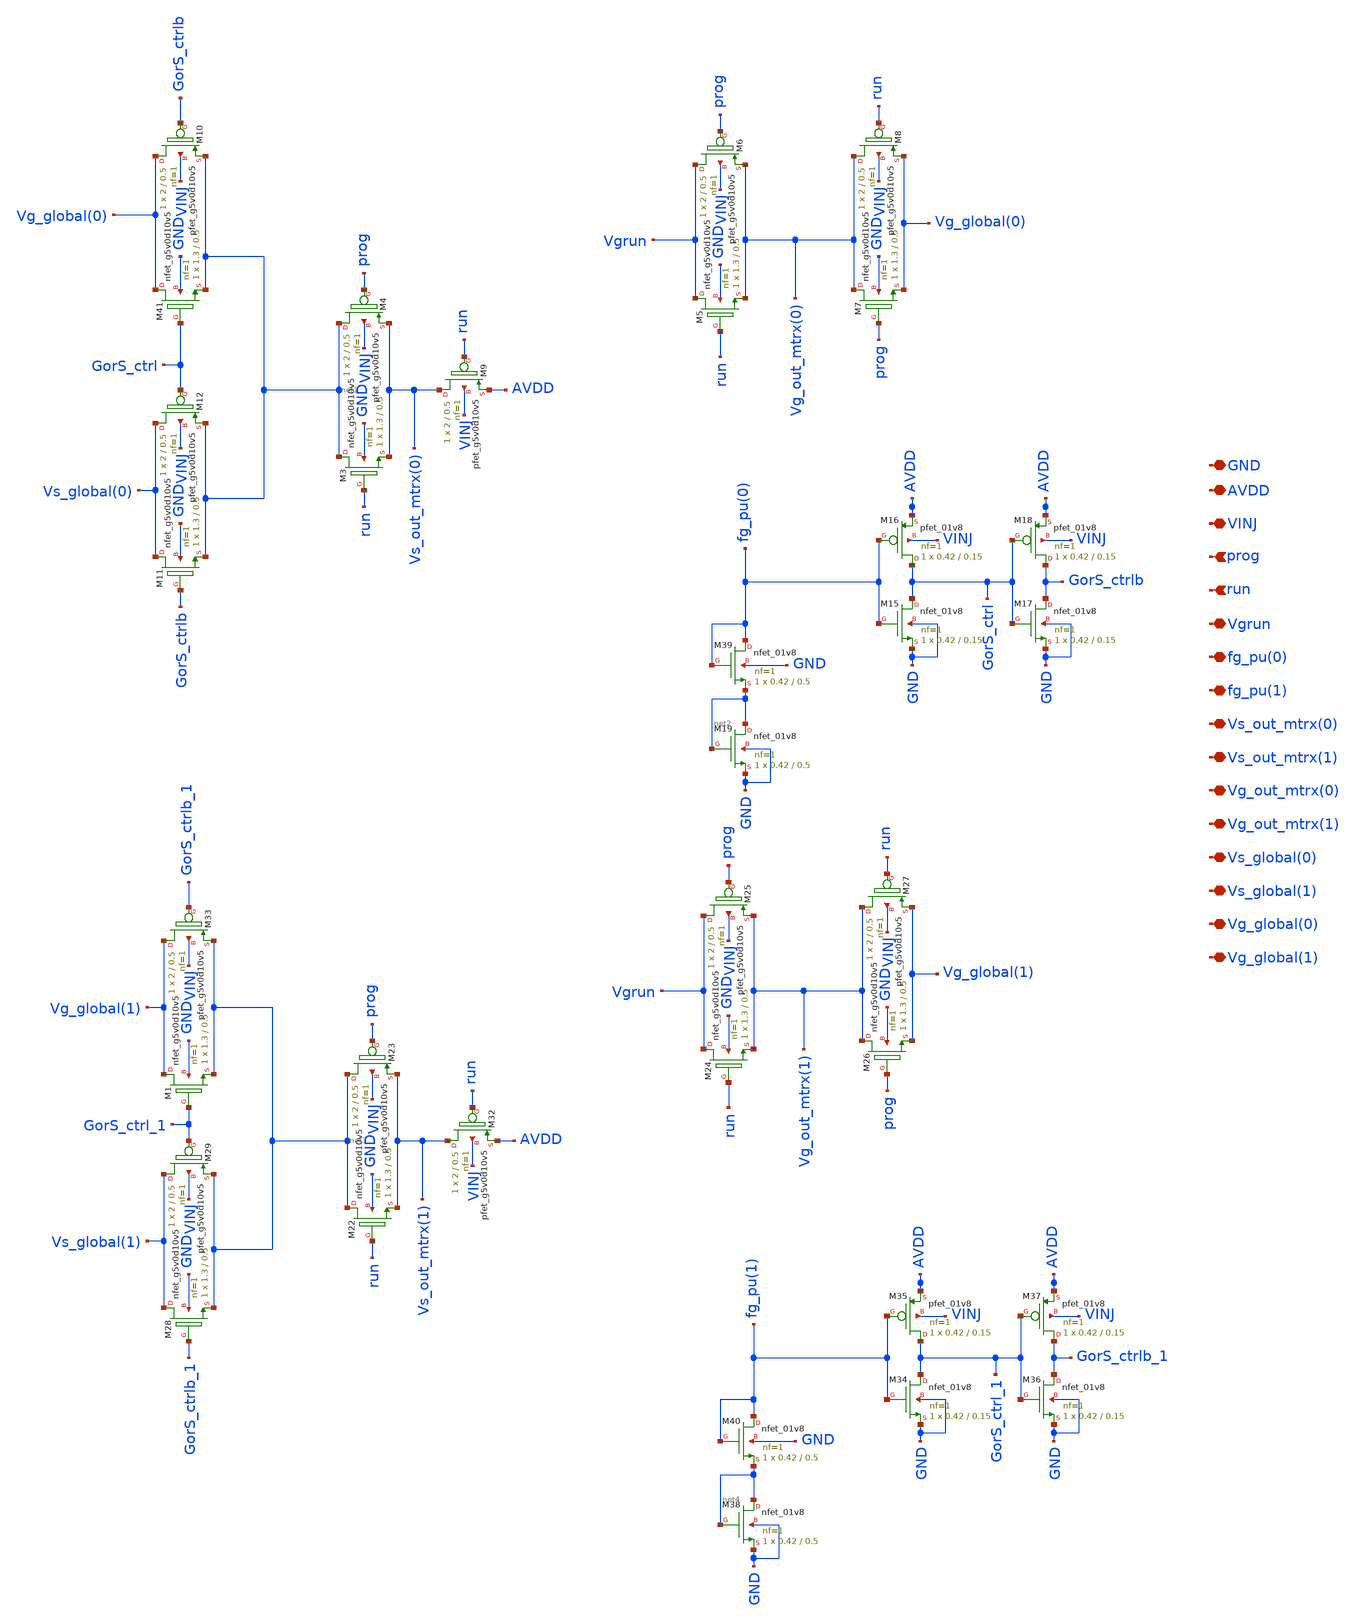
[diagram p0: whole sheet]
** sch_path: sky130_cells/IndirctGswc_OutMat/IndirectGswc_OutMatSchem.sch
**.subckt IndirectGswc_OutMatSchem GND AVDD VINJ Vgrun fg_pu(0) fg_pu(1) Vs_out_mtrx(0)
*+ Vs_out_mtrx(1) Vg_out_mtrx(0) Vg_out_mtrx(1) Vg_global(0) Vg_global(1) prog run Vs_global(0) Vs_global(1)
*.iopin GND
*.iopin AVDD
*.iopin VINJ
*.iopin Vgrun
*.iopin fg_pu(0)
*.iopin fg_pu(1)
*.iopin Vs_out_mtrx(0)
*.iopin Vs_out_mtrx(1)
*.iopin Vg_out_mtrx(0)
*.iopin Vg_out_mtrx(1)
*.iopin Vg_global(0)
*.iopin Vg_global(1)
*.ipin prog
*.ipin run
*.iopin Vs_global(0)
*.iopin Vs_global(1)
XM3 net1 run Vs_out_mtrx(0) GND sky130_fd_pr__nfet_g5v0d10v5 L=0.5 W=1.3 nf=1 ad='int((1 + 1)/2) * 1.3 / 1 * 0.29'
+ as='int((1 + 2)/2) * 1.3 / 1 * 0.29' pd='2*int((1 + 1)/2) * (1.3 / 1 + 0.29)' ps='2*int((1 + 2)/2) * (1.3 / 1 + 0.29)'
+ nrd='0.29 / 1.3 ' nrs='0.29 / 1.3 ' sa=0 sb=0 sd=0 mult=1 m=1
XM4 net1 prog Vs_out_mtrx(0) VINJ sky130_fd_pr__pfet_g5v0d10v5 L=0.5 W=2 nf=1 ad='int((1 + 1)/2) * 2 / 1 * 0.29'
+ as='int((1 + 2)/2) * 2 / 1 * 0.29' pd='2*int((1 + 1)/2) * (2 / 1 + 0.29)' ps='2*int((1 + 2)/2) * (2 / 1 + 0.29)'
+ nrd='0.29 / 2 ' nrs='0.29 / 2 ' sa=0 sb=0 sd=0 mult=1 m=1
XM5 Vgrun run Vg_out_mtrx(0) GND sky130_fd_pr__nfet_g5v0d10v5 L=0.5 W=1.3 nf=1 ad='int((1 + 1)/2) * 1.3 / 1 * 0.29'
+ as='int((1 + 2)/2) * 1.3 / 1 * 0.29' pd='2*int((1 + 1)/2) * (1.3 / 1 + 0.29)' ps='2*int((1 + 2)/2) * (1.3 / 1 + 0.29)'
+ nrd='0.29 / 1.3 ' nrs='0.29 / 1.3 ' sa=0 sb=0 sd=0 mult=1 m=1
XM6 Vgrun prog Vg_out_mtrx(0) VINJ sky130_fd_pr__pfet_g5v0d10v5 L=0.5 W=2 nf=1 ad='int((1 + 1)/2) * 2 / 1 * 0.29'
+ as='int((1 + 2)/2) * 2 / 1 * 0.29' pd='2*int((1 + 1)/2) * (2 / 1 + 0.29)' ps='2*int((1 + 2)/2) * (2 / 1 + 0.29)'
+ nrd='0.29 / 2 ' nrs='0.29 / 2 ' sa=0 sb=0 sd=0 mult=1 m=1
XM7 Vg_out_mtrx(0) prog Vg_global(0) GND sky130_fd_pr__nfet_g5v0d10v5 L=0.5 W=1.3 nf=1 ad='int((1 + 1)/2) * 1.3 / 1 * 0.29'
+ as='int((1 + 2)/2) * 1.3 / 1 * 0.29' pd='2*int((1 + 1)/2) * (1.3 / 1 + 0.29)' ps='2*int((1 + 2)/2) * (1.3 / 1 + 0.29)'
+ nrd='0.29 / 1.3 ' nrs='0.29 / 1.3 ' sa=0 sb=0 sd=0 mult=1 m=1
XM8 Vg_out_mtrx(0) run Vg_global(0) VINJ sky130_fd_pr__pfet_g5v0d10v5 L=0.5 W=2 nf=1 ad='int((1 + 1)/2) * 2 / 1 * 0.29'
+ as='int((1 + 2)/2) * 2 / 1 * 0.29' pd='2*int((1 + 1)/2) * (2 / 1 + 0.29)' ps='2*int((1 + 2)/2) * (2 / 1 + 0.29)'
+ nrd='0.29 / 2 ' nrs='0.29 / 2 ' sa=0 sb=0 sd=0 mult=1 m=1
XM11 Vs_global(0) GorS_ctrlb net1 GND sky130_fd_pr__nfet_g5v0d10v5 L=0.5 W=1.3 nf=1 ad='int((1 + 1)/2) * 1.3 / 1 * 0.29'
+ as='int((1 + 2)/2) * 1.3 / 1 * 0.29' pd='2*int((1 + 1)/2) * (1.3 / 1 + 0.29)' ps='2*int((1 + 2)/2) * (1.3 / 1 + 0.29)'
+ nrd='0.29 / 1.3 ' nrs='0.29 / 1.3 ' sa=0 sb=0 sd=0 mult=1 m=1
XM12 Vs_global(0) GorS_ctrl net1 VINJ sky130_fd_pr__pfet_g5v0d10v5 L=0.5 W=2 nf=1 ad='int((1 + 1)/2) * 2 / 1 * 0.29'
+ as='int((1 + 2)/2) * 2 / 1 * 0.29' pd='2*int((1 + 1)/2) * (2 / 1 + 0.29)' ps='2*int((1 + 2)/2) * (2 / 1 + 0.29)'
+ nrd='0.29 / 2 ' nrs='0.29 / 2 ' sa=0 sb=0 sd=0 mult=1 m=1
XM9 Vs_out_mtrx(0) run AVDD VINJ sky130_fd_pr__pfet_g5v0d10v5 L=0.5 W=2 nf=1 ad='int((1 + 1)/2) * 2 / 1 * 0.29'
+ as='int((1 + 2)/2) * 2 / 1 * 0.29' pd='2*int((1 + 1)/2) * (2 / 1 + 0.29)' ps='2*int((1 + 2)/2) * (2 / 1 + 0.29)'
+ nrd='0.29 / 2 ' nrs='0.29 / 2 ' sa=0 sb=0 sd=0 mult=1 m=1
XM10 Vg_global(0) GorS_ctrlb net1 VINJ sky130_fd_pr__pfet_g5v0d10v5 L=0.5 W=2 nf=1 ad='int((1 + 1)/2) * 2 / 1 * 0.29'
+ as='int((1 + 2)/2) * 2 / 1 * 0.29' pd='2*int((1 + 1)/2) * (2 / 1 + 0.29)' ps='2*int((1 + 2)/2) * (2 / 1 + 0.29)'
+ nrd='0.29 / 2 ' nrs='0.29 / 2 ' sa=0 sb=0 sd=0 mult=1 m=1
XM15 GorS_ctrl fg_pu(0) GND GND sky130_fd_pr__nfet_01v8 L=0.15 W=0.42 nf=1 ad='int((1 + 1)/2) * 0.42 / 1 * 0.29'
+ as='int((1 + 2)/2) * 0.42 / 1 * 0.29' pd='2*int((1 + 1)/2) * (0.42 / 1 + 0.29)' ps='2*int((1 + 2)/2) * (0.42 / 1 + 0.29)'
+ nrd='0.29 / 0.42 ' nrs='0.29 / 0.42 ' sa=0 sb=0 sd=0 mult=1 m=1
XM16 GorS_ctrl fg_pu(0) AVDD VINJ sky130_fd_pr__pfet_01v8 L=0.15 W=0.42 nf=1 ad='int((1 + 1)/2) * 0.42 / 1 * 0.29'
+ as='int((1 + 2)/2) * 0.42 / 1 * 0.29' pd='2*int((1 + 1)/2) * (0.42 / 1 + 0.29)' ps='2*int((1 + 2)/2) * (0.42 / 1 + 0.29)'
+ nrd='0.29 / 0.42 ' nrs='0.29 / 0.42 ' sa=0 sb=0 sd=0 mult=1 m=1
XM19 net2 net2 GND GND sky130_fd_pr__nfet_01v8 L=0.5 W=0.42 nf=1 ad='int((1 + 1)/2) * 0.42 / 1 * 0.29'
+ as='int((1 + 2)/2) * 0.42 / 1 * 0.29' pd='2*int((1 + 1)/2) * (0.42 / 1 + 0.29)' ps='2*int((1 + 2)/2) * (0.42 / 1 + 0.29)'
+ nrd='0.29 / 0.42 ' nrs='0.29 / 0.42 ' sa=0 sb=0 sd=0 mult=1 m=1
XM22 net3 run Vs_out_mtrx(1) GND sky130_fd_pr__nfet_g5v0d10v5 L=0.5 W=1.3 nf=1 ad='int((1 + 1)/2) * 1.3 / 1 * 0.29'
+ as='int((1 + 2)/2) * 1.3 / 1 * 0.29' pd='2*int((1 + 1)/2) * (1.3 / 1 + 0.29)' ps='2*int((1 + 2)/2) * (1.3 / 1 + 0.29)'
+ nrd='0.29 / 1.3 ' nrs='0.29 / 1.3 ' sa=0 sb=0 sd=0 mult=1 m=1
XM23 net3 prog Vs_out_mtrx(1) VINJ sky130_fd_pr__pfet_g5v0d10v5 L=0.5 W=2 nf=1 ad='int((1 + 1)/2) * 2 / 1 * 0.29'
+ as='int((1 + 2)/2) * 2 / 1 * 0.29' pd='2*int((1 + 1)/2) * (2 / 1 + 0.29)' ps='2*int((1 + 2)/2) * (2 / 1 + 0.29)'
+ nrd='0.29 / 2 ' nrs='0.29 / 2 ' sa=0 sb=0 sd=0 mult=1 m=1
XM24 Vgrun run Vg_out_mtrx(1) GND sky130_fd_pr__nfet_g5v0d10v5 L=0.5 W=1.3 nf=1 ad='int((1 + 1)/2) * 1.3 / 1 * 0.29'
+ as='int((1 + 2)/2) * 1.3 / 1 * 0.29' pd='2*int((1 + 1)/2) * (1.3 / 1 + 0.29)' ps='2*int((1 + 2)/2) * (1.3 / 1 + 0.29)'
+ nrd='0.29 / 1.3 ' nrs='0.29 / 1.3 ' sa=0 sb=0 sd=0 mult=1 m=1
XM25 Vgrun prog Vg_out_mtrx(1) VINJ sky130_fd_pr__pfet_g5v0d10v5 L=0.5 W=2 nf=1 ad='int((1 + 1)/2) * 2 / 1 * 0.29'
+ as='int((1 + 2)/2) * 2 / 1 * 0.29' pd='2*int((1 + 1)/2) * (2 / 1 + 0.29)' ps='2*int((1 + 2)/2) * (2 / 1 + 0.29)'
+ nrd='0.29 / 2 ' nrs='0.29 / 2 ' sa=0 sb=0 sd=0 mult=1 m=1
XM26 Vg_out_mtrx(1) prog Vg_global(1) GND sky130_fd_pr__nfet_g5v0d10v5 L=0.5 W=1.3 nf=1 ad='int((1 + 1)/2) * 1.3 / 1 * 0.29'
+ as='int((1 + 2)/2) * 1.3 / 1 * 0.29' pd='2*int((1 + 1)/2) * (1.3 / 1 + 0.29)' ps='2*int((1 + 2)/2) * (1.3 / 1 + 0.29)'
+ nrd='0.29 / 1.3 ' nrs='0.29 / 1.3 ' sa=0 sb=0 sd=0 mult=1 m=1
XM27 Vg_out_mtrx(1) run Vg_global(1) VINJ sky130_fd_pr__pfet_g5v0d10v5 L=0.5 W=2 nf=1 ad='int((1 + 1)/2) * 2 / 1 * 0.29'
+ as='int((1 + 2)/2) * 2 / 1 * 0.29' pd='2*int((1 + 1)/2) * (2 / 1 + 0.29)' ps='2*int((1 + 2)/2) * (2 / 1 + 0.29)'
+ nrd='0.29 / 2 ' nrs='0.29 / 2 ' sa=0 sb=0 sd=0 mult=1 m=1
XM28 Vs_global(1) GorS_ctrlb_1 net3 GND sky130_fd_pr__nfet_g5v0d10v5 L=0.5 W=1.3 nf=1 ad='int((1 + 1)/2) * 1.3 / 1 * 0.29'
+ as='int((1 + 2)/2) * 1.3 / 1 * 0.29' pd='2*int((1 + 1)/2) * (1.3 / 1 + 0.29)' ps='2*int((1 + 2)/2) * (1.3 / 1 + 0.29)'
+ nrd='0.29 / 1.3 ' nrs='0.29 / 1.3 ' sa=0 sb=0 sd=0 mult=1 m=1
XM29 Vs_global(1) GorS_ctrl_1 net3 VINJ sky130_fd_pr__pfet_g5v0d10v5 L=0.5 W=2 nf=1 ad='int((1 + 1)/2) * 2 / 1 * 0.29'
+ as='int((1 + 2)/2) * 2 / 1 * 0.29' pd='2*int((1 + 1)/2) * (2 / 1 + 0.29)' ps='2*int((1 + 2)/2) * (2 / 1 + 0.29)'
+ nrd='0.29 / 2 ' nrs='0.29 / 2 ' sa=0 sb=0 sd=0 mult=1 m=1
XM32 Vs_out_mtrx(1) run AVDD VINJ sky130_fd_pr__pfet_g5v0d10v5 L=0.5 W=2 nf=1 ad='int((1 + 1)/2) * 2 / 1 * 0.29'
+ as='int((1 + 2)/2) * 2 / 1 * 0.29' pd='2*int((1 + 1)/2) * (2 / 1 + 0.29)' ps='2*int((1 + 2)/2) * (2 / 1 + 0.29)'
+ nrd='0.29 / 2 ' nrs='0.29 / 2 ' sa=0 sb=0 sd=0 mult=1 m=1
XM33 Vg_global(1) GorS_ctrlb_1 net3 VINJ sky130_fd_pr__pfet_g5v0d10v5 L=0.5 W=2 nf=1 ad='int((1 + 1)/2) * 2 / 1 * 0.29'
+ as='int((1 + 2)/2) * 2 / 1 * 0.29' pd='2*int((1 + 1)/2) * (2 / 1 + 0.29)' ps='2*int((1 + 2)/2) * (2 / 1 + 0.29)'
+ nrd='0.29 / 2 ' nrs='0.29 / 2 ' sa=0 sb=0 sd=0 mult=1 m=1
XM17 GorS_ctrlb GorS_ctrl GND GND sky130_fd_pr__nfet_01v8 L=0.15 W=0.42 nf=1 ad='int((1 + 1)/2) * 0.42 / 1 * 0.29'
+ as='int((1 + 2)/2) * 0.42 / 1 * 0.29' pd='2*int((1 + 1)/2) * (0.42 / 1 + 0.29)' ps='2*int((1 + 2)/2) * (0.42 / 1 + 0.29)'
+ nrd='0.29 / 0.42 ' nrs='0.29 / 0.42 ' sa=0 sb=0 sd=0 mult=1 m=1
XM18 GorS_ctrlb GorS_ctrl AVDD VINJ sky130_fd_pr__pfet_01v8 L=0.15 W=0.42 nf=1 ad='int((1 + 1)/2) * 0.42 / 1 * 0.29'
+ as='int((1 + 2)/2) * 0.42 / 1 * 0.29' pd='2*int((1 + 1)/2) * (0.42 / 1 + 0.29)' ps='2*int((1 + 2)/2) * (0.42 / 1 + 0.29)'
+ nrd='0.29 / 0.42 ' nrs='0.29 / 0.42 ' sa=0 sb=0 sd=0 mult=1 m=1
XM34 GorS_ctrl_1 fg_pu(1) GND GND sky130_fd_pr__nfet_01v8 L=0.15 W=0.42 nf=1 ad='int((1 + 1)/2) * 0.42 / 1 * 0.29'
+ as='int((1 + 2)/2) * 0.42 / 1 * 0.29' pd='2*int((1 + 1)/2) * (0.42 / 1 + 0.29)' ps='2*int((1 + 2)/2) * (0.42 / 1 + 0.29)'
+ nrd='0.29 / 0.42 ' nrs='0.29 / 0.42 ' sa=0 sb=0 sd=0 mult=1 m=1
XM35 GorS_ctrl_1 fg_pu(1) AVDD VINJ sky130_fd_pr__pfet_01v8 L=0.15 W=0.42 nf=1 ad='int((1 + 1)/2) * 0.42 / 1 * 0.29'
+ as='int((1 + 2)/2) * 0.42 / 1 * 0.29' pd='2*int((1 + 1)/2) * (0.42 / 1 + 0.29)' ps='2*int((1 + 2)/2) * (0.42 / 1 + 0.29)'
+ nrd='0.29 / 0.42 ' nrs='0.29 / 0.42 ' sa=0 sb=0 sd=0 mult=1 m=1
XM36 GorS_ctrlb_1 GorS_ctrl_1 GND GND sky130_fd_pr__nfet_01v8 L=0.15 W=0.42 nf=1 ad='int((1 + 1)/2) * 0.42 / 1 * 0.29'
+ as='int((1 + 2)/2) * 0.42 / 1 * 0.29' pd='2*int((1 + 1)/2) * (0.42 / 1 + 0.29)' ps='2*int((1 + 2)/2) * (0.42 / 1 + 0.29)'
+ nrd='0.29 / 0.42 ' nrs='0.29 / 0.42 ' sa=0 sb=0 sd=0 mult=1 m=1
XM37 GorS_ctrlb_1 GorS_ctrl_1 AVDD VINJ sky130_fd_pr__pfet_01v8 L=0.15 W=0.42 nf=1 ad='int((1 + 1)/2) * 0.42 / 1 * 0.29'
+ as='int((1 + 2)/2) * 0.42 / 1 * 0.29' pd='2*int((1 + 1)/2) * (0.42 / 1 + 0.29)' ps='2*int((1 + 2)/2) * (0.42 / 1 + 0.29)'
+ nrd='0.29 / 0.42 ' nrs='0.29 / 0.42 ' sa=0 sb=0 sd=0 mult=1 m=1
XM39 fg_pu(0) fg_pu(0) net2 GND sky130_fd_pr__nfet_01v8 L=0.5 W=0.42 nf=1 ad='int((1 + 1)/2) * 0.42 / 1 * 0.29'
+ as='int((1 + 2)/2) * 0.42 / 1 * 0.29' pd='2*int((1 + 1)/2) * (0.42 / 1 + 0.29)' ps='2*int((1 + 2)/2) * (0.42 / 1 + 0.29)'
+ nrd='0.29 / 0.42 ' nrs='0.29 / 0.42 ' sa=0 sb=0 sd=0 mult=1 m=1
XM38 net4 net4 GND GND sky130_fd_pr__nfet_01v8 L=0.5 W=0.42 nf=1 ad='int((1 + 1)/2) * 0.42 / 1 * 0.29'
+ as='int((1 + 2)/2) * 0.42 / 1 * 0.29' pd='2*int((1 + 1)/2) * (0.42 / 1 + 0.29)' ps='2*int((1 + 2)/2) * (0.42 / 1 + 0.29)'
+ nrd='0.29 / 0.42 ' nrs='0.29 / 0.42 ' sa=0 sb=0 sd=0 mult=1 m=1
XM40 fg_pu(1) fg_pu(1) net4 GND sky130_fd_pr__nfet_01v8 L=0.5 W=0.42 nf=1 ad='int((1 + 1)/2) * 0.42 / 1 * 0.29'
+ as='int((1 + 2)/2) * 0.42 / 1 * 0.29' pd='2*int((1 + 1)/2) * (0.42 / 1 + 0.29)' ps='2*int((1 + 2)/2) * (0.42 / 1 + 0.29)'
+ nrd='0.29 / 0.42 ' nrs='0.29 / 0.42 ' sa=0 sb=0 sd=0 mult=1 m=1
XM41 Vg_global(0) GorS_ctrl net1 GND sky130_fd_pr__nfet_g5v0d10v5 L=0.5 W=1.3 nf=1 ad='int((1 + 1)/2) * 1.3 / 1 * 0.29'
+ as='int((1 + 2)/2) * 1.3 / 1 * 0.29' pd='2*int((1 + 1)/2) * (1.3 / 1 + 0.29)' ps='2*int((1 + 2)/2) * (1.3 / 1 + 0.29)'
+ nrd='0.29 / 1.3 ' nrs='0.29 / 1.3 ' sa=0 sb=0 sd=0 mult=1 m=1
XM1 Vg_global(1) GorS_ctrl_1 net3 GND sky130_fd_pr__nfet_g5v0d10v5 L=0.5 W=1.3 nf=1 ad='int((1 + 1)/2) * 1.3 / 1 * 0.29'
+ as='int((1 + 2)/2) * 1.3 / 1 * 0.29' pd='2*int((1 + 1)/2) * (1.3 / 1 + 0.29)' ps='2*int((1 + 2)/2) * (1.3 / 1 + 0.29)'
+ nrd='0.29 / 1.3 ' nrs='0.29 / 1.3 ' sa=0 sb=0 sd=0 mult=1 m=1
**.ends
.end
